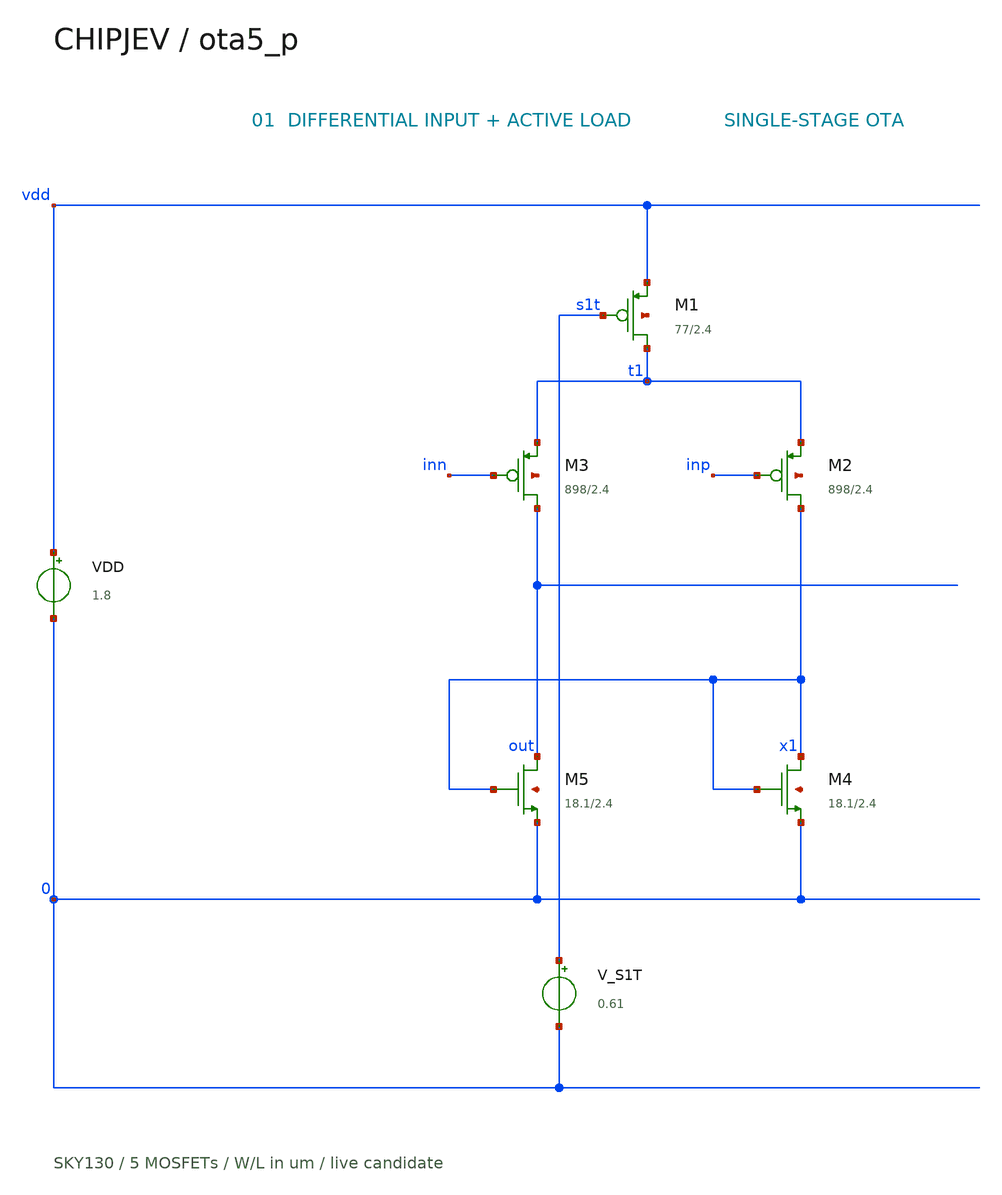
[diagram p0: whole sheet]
** sch_path: experiments/analog-layout/ota-efficient/circuit.sch
**.subckt circuit
VDD vdd 0 1.8
XM1 t1 s1t vdd vdd sky130_fd_pr__pfet_01v8 L=2.4 W=77.04 nf=2 ad=11.1708 as=22.3416 pd=77.62
+ ps=155.24 nrd=0.00376428 nrs=0.00376428 sa=0 sb=0 sd=0 mult=1 m=1
XM2 x1 inp t1 vdd sky130_fd_pr__pfet_01v8 L=2.4 W=897.66 nf=18 ad=130.161 as=144.623 pd=902.88
+ ps=1003.2 nrd=0.000323062 nrs=0.000323062 sa=0 sb=0 sd=0 mult=1 m=1
XM3 out inn t1 vdd sky130_fd_pr__pfet_01v8 L=2.4 W=897.66 nf=18 ad=130.161 as=144.623 pd=902.88
+ ps=1003.2 nrd=0.000323062 nrs=0.000323062 sa=0 sb=0 sd=0 mult=1 m=1
XM4 x1 x1 0 0 sky130_fd_pr__nfet_01v8 L=2.4 W=18.14 nf=1 ad=5.2606 as=5.2606 pd=36.86 ps=36.86
+ nrd=0.0159868 nrs=0.0159868 sa=0 sb=0 sd=0 mult=1 m=1
XM5 out x1 0 0 sky130_fd_pr__nfet_01v8 L=2.4 W=18.14 nf=1 ad=5.2606 as=5.2606 pd=36.86 ps=36.86
+ nrd=0.0159868 nrs=0.0159868 sa=0 sb=0 sd=0 mult=1 m=1
V_S1T s1t 0 0.61
**.ends
.end
